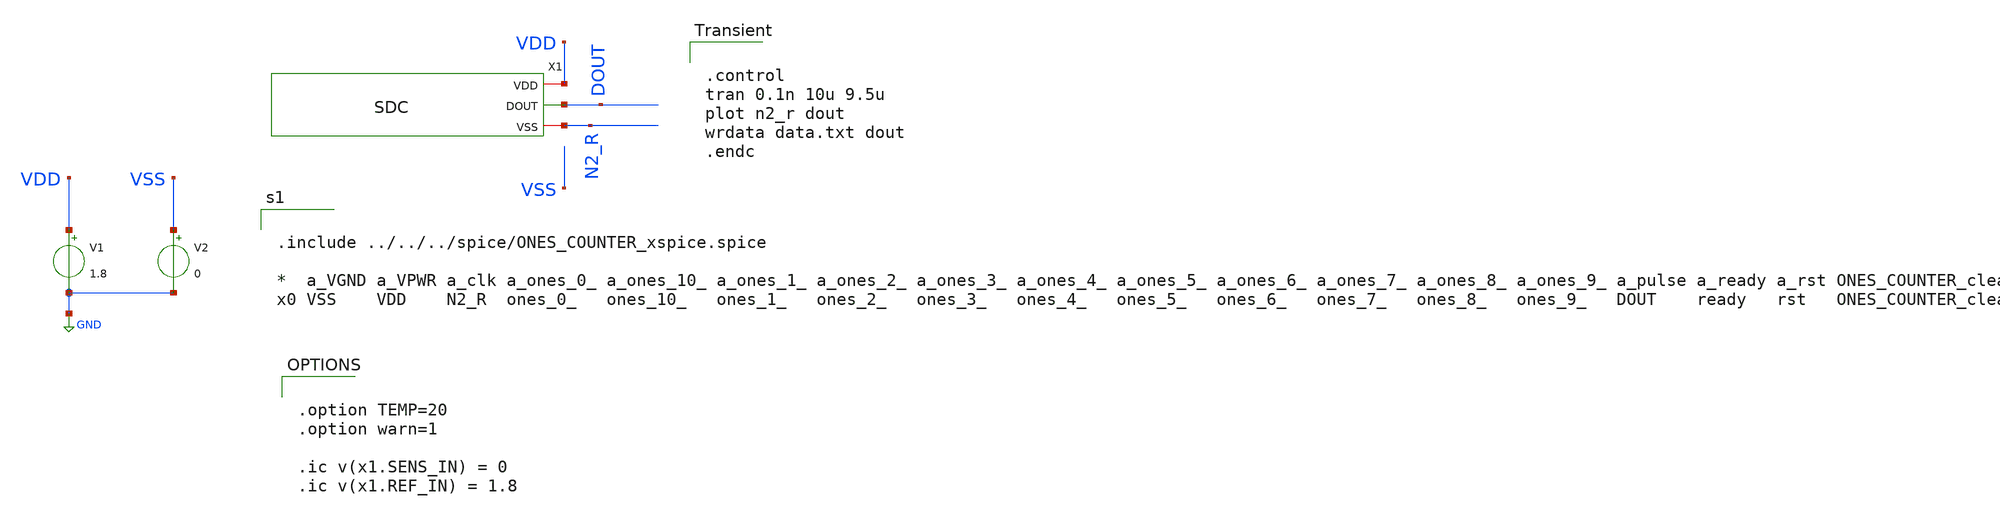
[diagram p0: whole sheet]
** sch_path: modules/ONES_COUNTER/test/transient.sch
**.subckt transient
V1 VDD GND 1.8
V2 VSS GND 0
X1 VDD DOUT N2_R SDC
**** begin user architecture code


.control
tran 0.1n 10u 9.5u
plot n2_r dout
wrdata data.txt dout
.endc



.option TEMP=20
.option warn=1

.ic v(x1.SENS_IN) = 0
.ic v(x1.REF_IN) = 1.8



.lib $env(PDK_ROOT)/$env(PDK)/libs.tech/ngspice/sky130.lib.spice.tt.red tt

.include $env(PDK_ROOT)/$env(PDK)/libs.ref/sky130_fd_sc_hd/spice/sky130_fd_sc_hd.spice



.include ../../../spice/ONES_COUNTER_xspice.spice

*  a_VGND a_VPWR a_clk a_ones_0_ a_ones_10_ a_ones_1_ a_ones_2_ a_ones_3_ a_ones_4_ a_ones_5_
*+ a_ones_6_ a_ones_7_ a_ones_8_ a_ones_9_ a_pulse a_ready a_rst ONES_COUNTER_clean
x0 VSS    VDD    N2_R  ones_0_   ones_10_   ones_1_   ones_2_   ones_3_   ones_4_   ones_5_
+   ones_6_   ones_7_   ones_8_   ones_9_   DOUT    ready   rst   ONES_COUNTER_clean


**** end user architecture code
**.ends
.GLOBAL GND
.end
